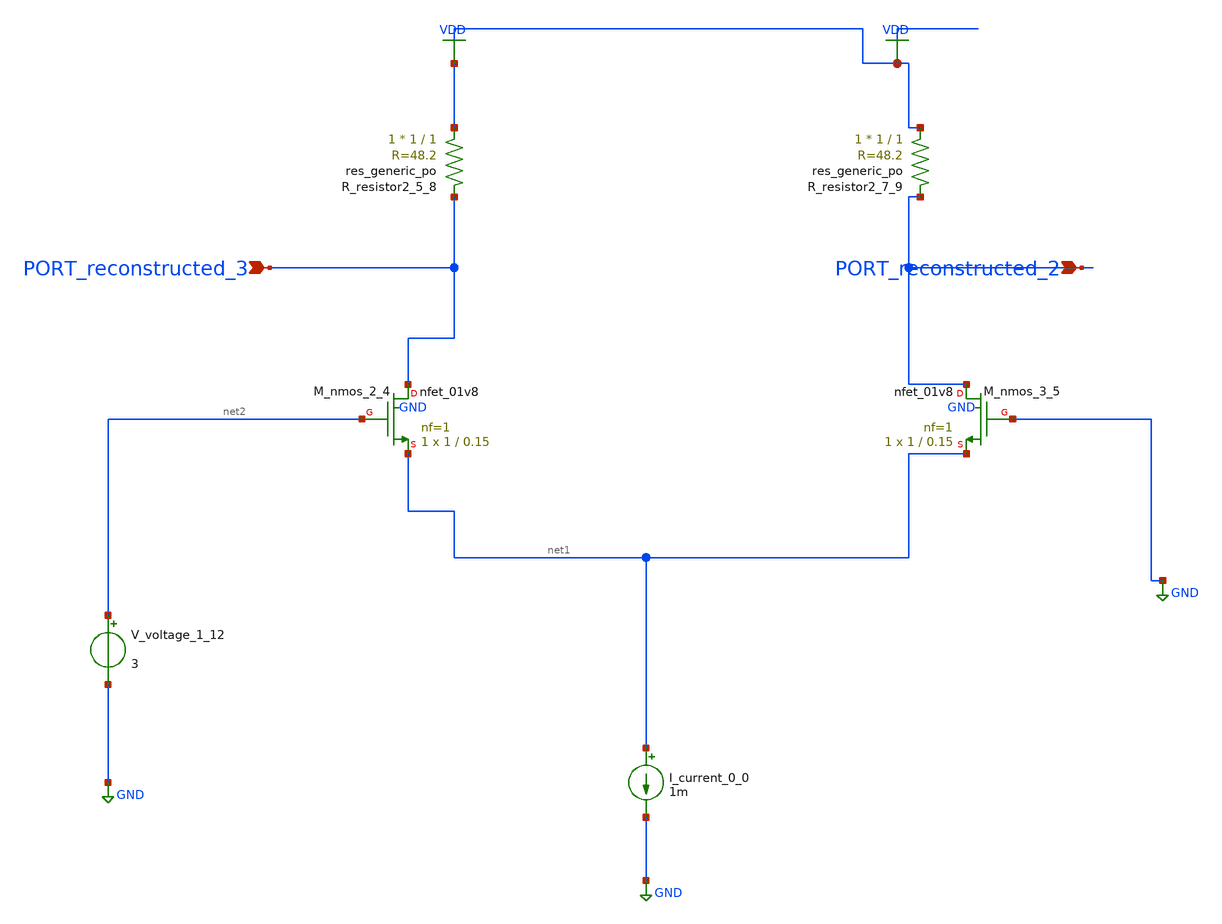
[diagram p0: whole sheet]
** sch_path: schematics/AMSNet/196.sch
**.subckt 196 PORT_reconstructed_2 PORT_reconstructed_3
*.ipin PORT_reconstructed_2
*.ipin PORT_reconstructed_3
I_current_0_0 net1 GND 1m
XM_nmos_2_4 PORT_reconstructed_3 net2 net1 GND sky130_fd_pr__nfet_01v8 L=0.15 W=1 nf=1 ad='int((1 + 1)/2) * 1 / 1 * 0.29'
+ as='int((1 + 2)/2) * 1 / 1 * 0.29' pd='2*int((1 + 1)/2) * (1 / 1 + 0.29)' ps='2*int((1 + 2)/2) * (1 / 1 + 0.29)'
+ nrd='0.29 / 1 ' nrs='0.29 / 1 ' sa=0 sb=0 sd=0 mult=1 m=1
XM_nmos_3_5 PORT_reconstructed_2 GND net1 GND sky130_fd_pr__nfet_01v8 L=0.15 W=1 nf=1 ad='int((1 + 1)/2) * 1 / 1 * 0.29'
+ as='int((1 + 2)/2) * 1 / 1 * 0.29' pd='2*int((1 + 1)/2) * (1 / 1 + 0.29)' ps='2*int((1 + 2)/2) * (1 / 1 + 0.29)'
+ nrd='0.29 / 1 ' nrs='0.29 / 1 ' sa=0 sb=0 sd=0 mult=1 m=1
XR_resistor2_5_8 VDD PORT_reconstructed_3 sky130_fd_pr__res_generic_po W=1 L=1 m=1
XR_resistor2_7_9 VDD PORT_reconstructed_2 sky130_fd_pr__res_generic_po W=1 L=1 m=1
V_voltage_1_12 net2 GND 3
**.ends
.GLOBAL GND
.GLOBAL VDD
.end
